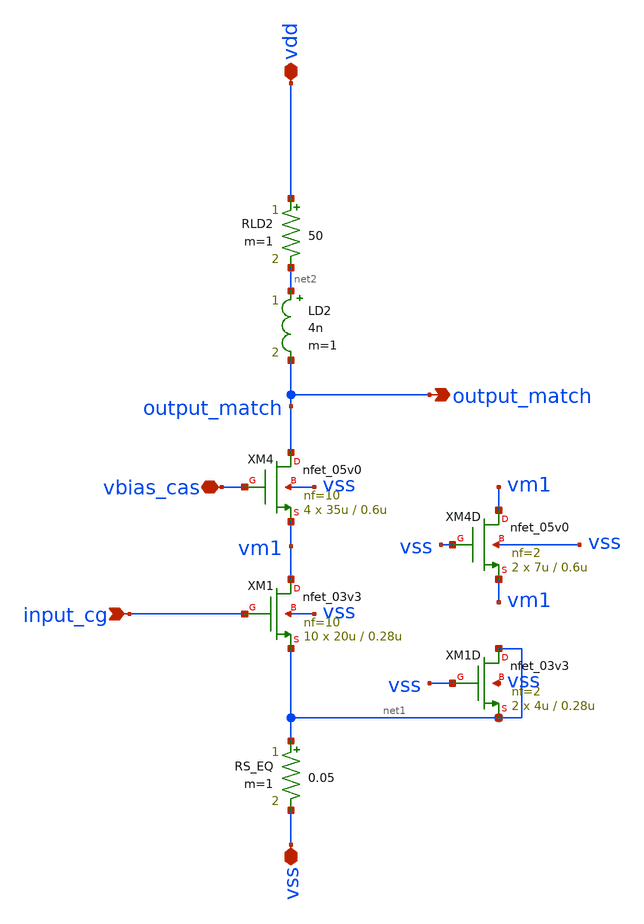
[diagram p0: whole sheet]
** sch_path: xschem/lna_core_cs.sch
**.subckt lna_core_cs vbias_cas input_cg output_match vdd vss
*.iopin vbias_cas
*.ipin input_cg
*.opin output_match
*.iopin vdd
*.iopin vss
XM4 output_match vbias_cas vm1 vss nfet_05v0 L=0.6u W=35u nf=10 ad='int((nf+1)/2) * W/nf * 0.18u' as='int((nf+2)/2) * W/nf * 0.18u'
+ pd='2*int((nf+1)/2) * (W/nf + 0.18u)' ps='2*int((nf+2)/2) * (W/nf + 0.18u)' nrd='0.18u / W' nrs='0.18u / W'
+ sa=0 sb=0 sd=0 m=4
RS_EQ net1 vss 0.05 m=1
XM1 vm1 input_cg net1 vss nfet_03v3 L=0.28u W=20u nf=10 ad='int((nf+1)/2) * W/nf * 0.18u' as='int((nf+2)/2) * W/nf * 0.18u'
+ pd='2*int((nf+1)/2) * (W/nf + 0.18u)' ps='2*int((nf+2)/2) * (W/nf + 0.18u)' nrd='0.18u / W' nrs='0.18u / W'
+ sa=0 sb=0 sd=0 m=10
LD2 net2 output_match 4n m=1
RLD2 vdd net2 50 m=1
XM1D net1 vss net1 vss nfet_03v3 L=0.28u W=4u nf=2 ad='int((nf+1)/2) * W/nf * 0.18u' as='int((nf+2)/2) * W/nf * 0.18u'
+ pd='2*int((nf+1)/2) * (W/nf + 0.18u)' ps='2*int((nf+2)/2) * (W/nf + 0.18u)' nrd='0.18u / W' nrs='0.18u / W'
+ sa=0 sb=0 sd=0 m=2
XM4D vm1 vss vm1 vss nfet_05v0 L=0.6u W=7u nf=2 ad='int((nf+1)/2) * W/nf * 0.18u' as='int((nf+2)/2) * W/nf * 0.18u'
+ pd='2*int((nf+1)/2) * (W/nf + 0.18u)' ps='2*int((nf+2)/2) * (W/nf + 0.18u)' nrd='0.18u / W' nrs='0.18u / W'
+ sa=0 sb=0 sd=0 m=2
**.ends
.end
